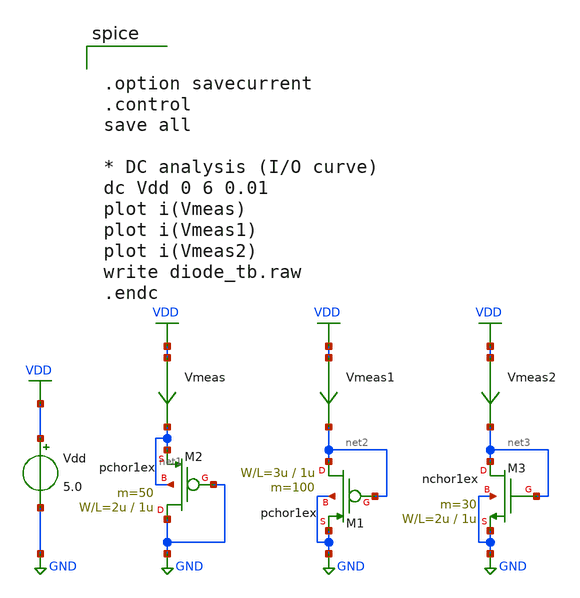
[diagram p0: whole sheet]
** sch_path: design/xschem/diode.sch
**.subckt diode
Vmeas VDD net1 0
.save i(vmeas)
Vdd VDD GND 5.0
M2 GND GND net1 net1 pchor1ex L=1u W=2u m=50
Vmeas1 VDD net2 0
.save i(vmeas1)
M1 net2 net2 GND GND pchor1ex L=1u W=3u m=100
Vmeas2 VDD net3 0
.save i(vmeas2)
M3 net3 net3 GND GND nchor1ex L=1u W=2u m=30
**** begin user architecture code


.option savecurrent
.control
save all

* DC analysis (I/O curve)
dc Vdd 0 6 0.01
plot i(Vmeas)
plot i(Vmeas1)
plot i(Vmeas2)
write diode_tb.raw
.endc

 .include $::LIB/mos.lib
.include $::LIB/passive.lib
.include $::LIB/diode.lib
**** end user architecture code
**.ends
.GLOBAL VDD
.GLOBAL GND
.end
